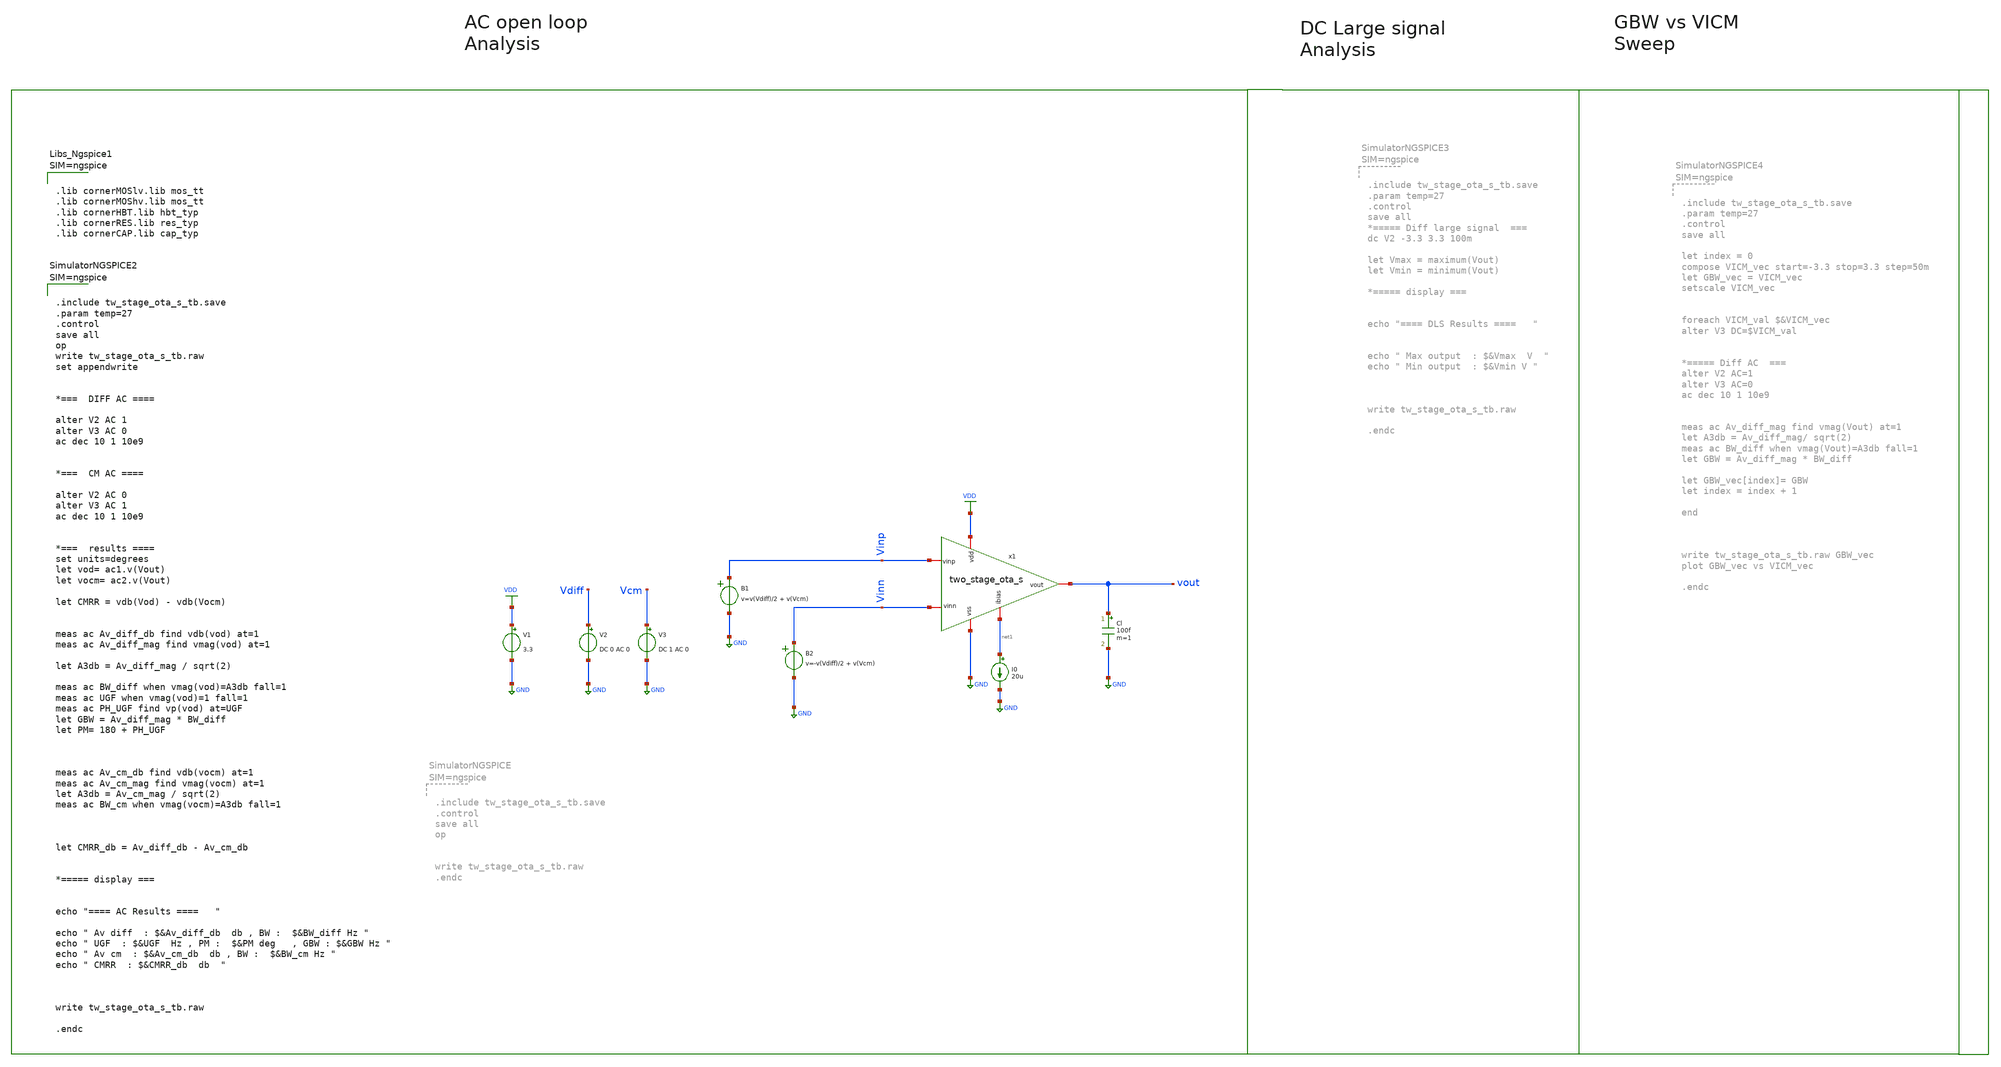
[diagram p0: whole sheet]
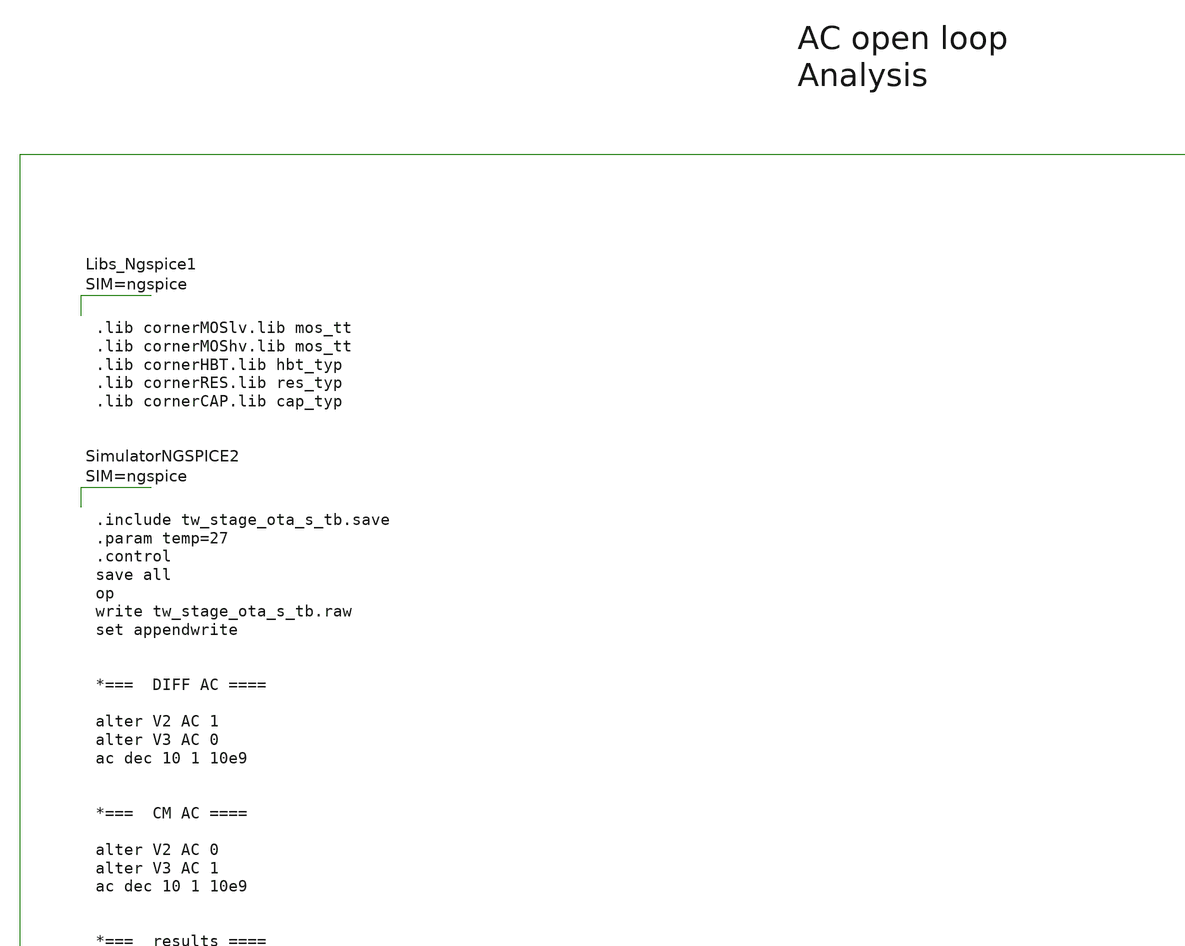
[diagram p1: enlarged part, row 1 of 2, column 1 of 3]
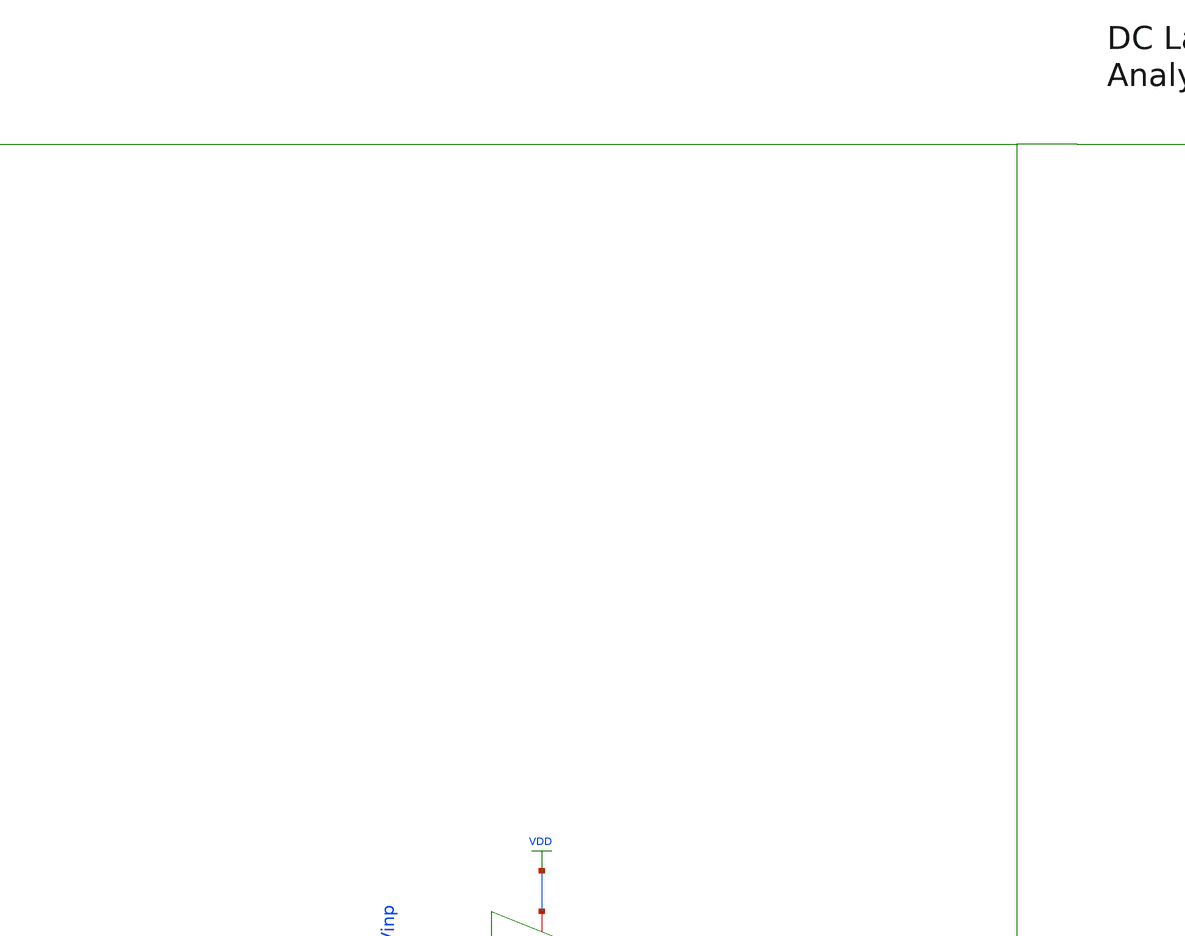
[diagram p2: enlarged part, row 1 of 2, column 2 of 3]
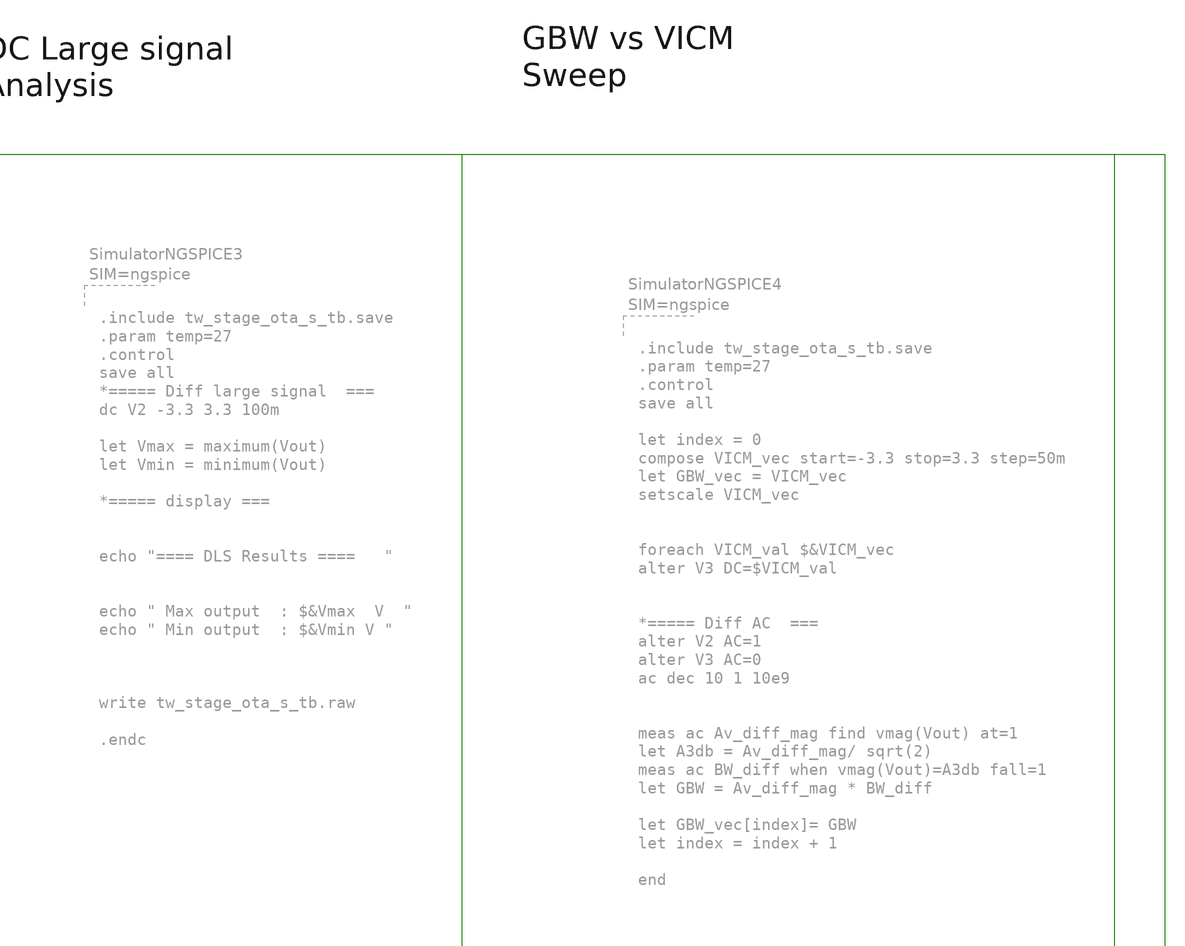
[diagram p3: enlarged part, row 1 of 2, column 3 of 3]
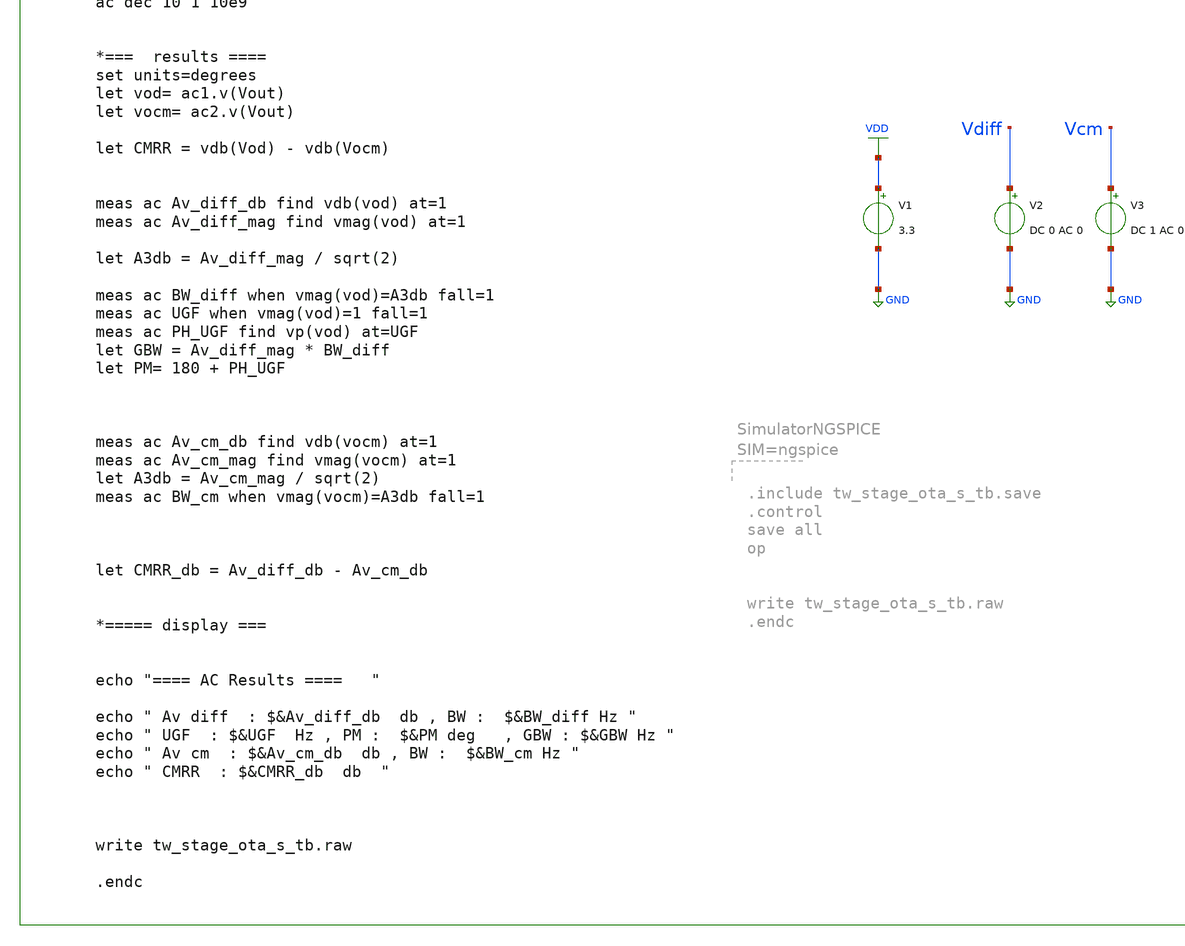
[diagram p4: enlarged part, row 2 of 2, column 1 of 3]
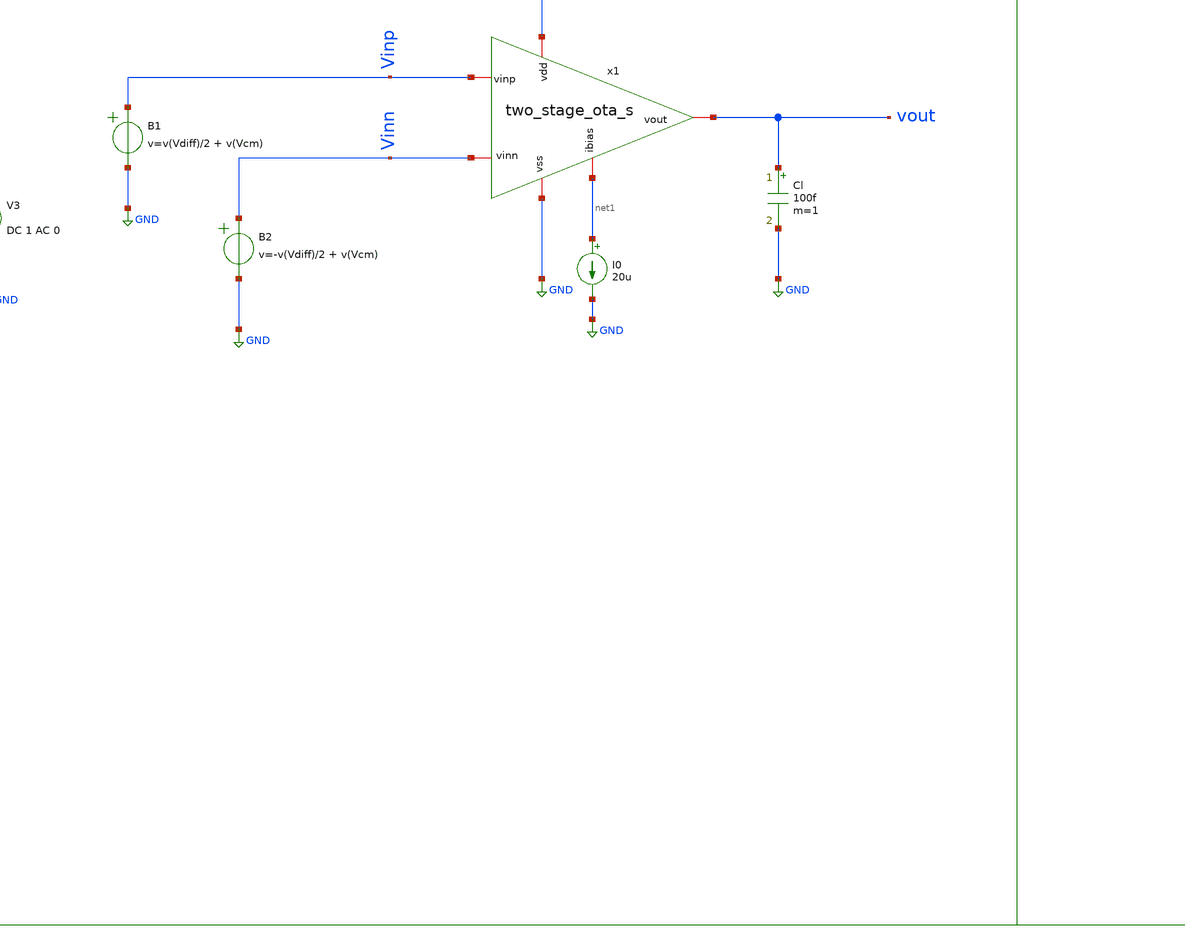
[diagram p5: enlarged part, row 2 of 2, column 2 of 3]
** sch_path: dependencies/pmu_ip/dependencies/OTA/OTA-main/testbenches/tw_stage_ota_s_tb.sch
* (c) 2025-2026 Ider Abdelaziz
**.subckt tw_stage_ota_s_tb
I0 net1 GND 20u
Cl vout GND 100f m=1
B2 Vinn GND v=-v(Vdiff)/2 + v(Vcm)
V1 VDD GND 3.3
V2 Vdiff GND DC 0 AC 0
V3 Vcm GND DC 1 AC 0
B1 Vinp GND v=v(Vdiff)/2 + v(Vcm)
x1 VDD net1 Vinn Vinp vout GND two_stage_ota_s
**** begin user architecture code



.include tw_stage_ota_s_tb.save
.param temp=27
.control
save all
op
write tw_stage_ota_s_tb.raw
set appendwrite


*===  DIFF AC ====

alter V2 AC 1
alter V3 AC 0
ac dec 10 1 10e9


*===  CM AC ====

alter V2 AC 0
alter V3 AC 1
ac dec 10 1 10e9


*===  results ====
set units=degrees
let vod= ac1.v(Vout)
let vocm= ac2.v(Vout)

let CMRR = vdb(Vod) - vdb(Vocm)


meas ac Av_diff_db find vdb(vod) at=1
meas ac Av_diff_mag find vmag(vod) at=1

let A3db = Av_diff_mag / sqrt(2)

meas ac BW_diff when vmag(vod)=A3db fall=1
meas ac UGF when vmag(vod)=1 fall=1
meas ac PH_UGF find vp(vod) at=UGF
let GBW = Av_diff_mag * BW_diff
let PM= 180 + PH_UGF



meas ac Av_cm_db find vdb(vocm) at=1
meas ac Av_cm_mag find vmag(vocm) at=1
let A3db = Av_cm_mag / sqrt(2)
meas ac BW_cm when vmag(vocm)=A3db fall=1



let CMRR_db = Av_diff_db - Av_cm_db


*===== display ===


echo "==== AC Results ====   "

echo " Av diff  : $&Av_diff_db  db , BW :  $&BW_diff Hz "
echo " UGF  : $&UGF  Hz , PM :  $&PM deg   , GBW : $&GBW Hz "
echo " Av cm  : $&Av_cm_db  db , BW :  $&BW_cm Hz "
echo " CMRR  : $&CMRR_db  db  "



write tw_stage_ota_s_tb.raw

.endc






.lib cornerMOSlv.lib mos_tt
.lib cornerMOShv.lib mos_tt
.lib cornerHBT.lib hbt_typ
.lib cornerRES.lib res_typ
.lib cornerCAP.lib cap_typ



**** end user architecture code
**.ends

* expanding   symbol:  two_stage_ota_s.sym # of pins=6
** sym_path: dependencies/pmu_ip/dependencies/OTA/OTA-main/testbenches/two_stage_ota_s.sym
** sch_path: dependencies/pmu_ip/dependencies/OTA/OTA-main/testbenches/two_stage_ota_s.sch
.subckt two_stage_ota_s vdd ibias vinn vinp vout vss
*.iopin ibias
*.iopin vdd
*.iopin vss
*.iopin vout
*.iopin vinp
*.iopin vinn
C1 net4 vout 350f m=1
R1 net3 net4 4k m=1
XM4 net3 net2 vss vss sg13_hv_nmos w=3u l=1u ng=1 m=1 mm_ok=1
XM3 net2 net2 vss vss sg13_hv_nmos w=3u l=1u ng=1 m=1 mm_ok=1
XM1 net3 vinp net1 vdd sg13_hv_pmos w=12u l=1u ng=1 m=2 mm_ok=1
XM2 net2 vinn net1 vdd sg13_hv_pmos w=12u l=1u ng=1 m=2 mm_ok=1
XM5 net1 ibias vdd vdd sg13_hv_pmos w=6u l=3u ng=1 m=2 mm_ok=1
XM7 vout ibias vdd vdd sg13_hv_pmos w=6u l=3u ng=1 m=8 mm_ok=1
XM8 ibias ibias vdd vdd sg13_hv_pmos w=6u l=3u ng=1 m=8 mm_ok=1
XM9 vout net3 vss vss sg13_hv_nmos w=12u l=1u ng=1 m=2 mm_ok=1
.ends

.GLOBAL GND
.GLOBAL VDD
.end
